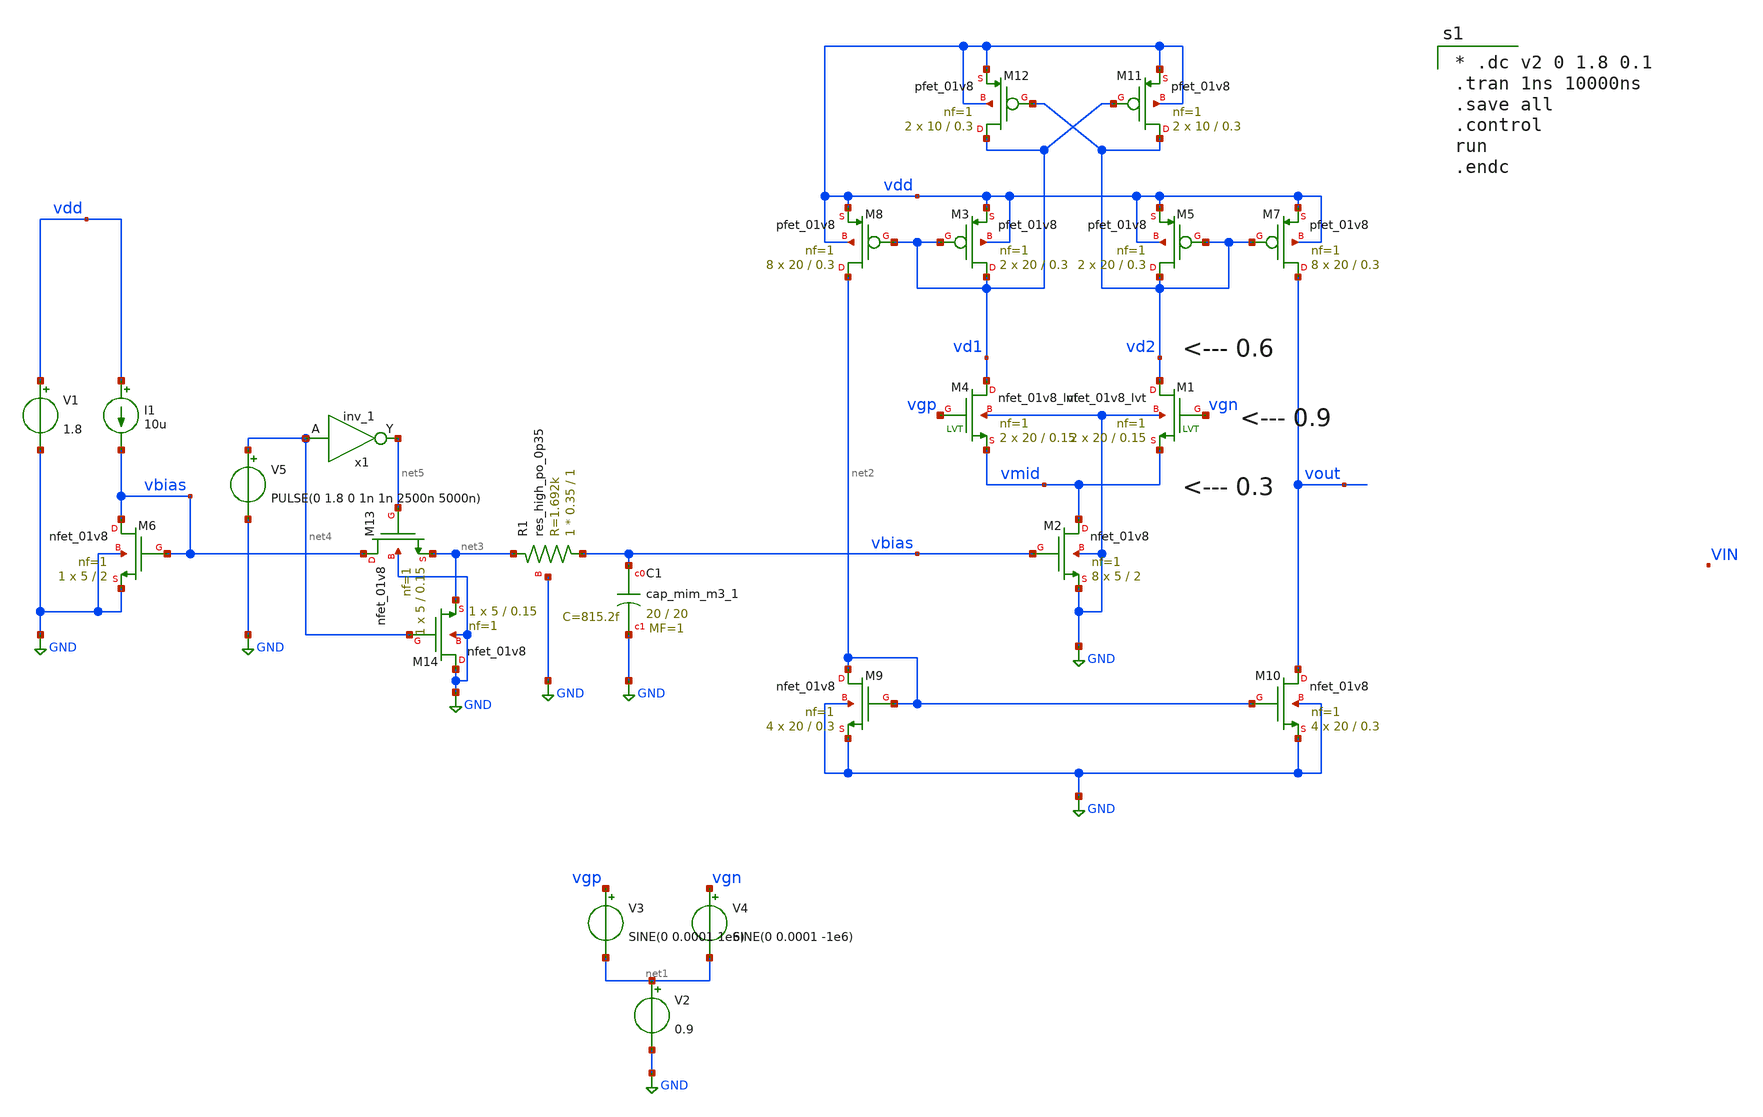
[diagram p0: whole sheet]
** sch_path: xschem/i_type_ota_tran_tb.sch
**.subckt i_type_ota_tran_tb
XM2 vmid vbias GND GND sky130_fd_pr__nfet_01v8 L=2 W=5 nf=1 ad='int((nf+1)/2) * W/nf * 0.29' as='int((nf+2)/2) * W/nf * 0.29'
+ pd='2*int((nf+1)/2) * (W/nf + 0.29)' ps='2*int((nf+2)/2) * (W/nf + 0.29)' nrd='0.29 / W' nrs='0.29 / W'
+ sa=0 sb=0 sd=0 mult=8 m=8
XM6 vbias vbias GND GND sky130_fd_pr__nfet_01v8 L=2 W=5 nf=1 ad='int((nf+1)/2) * W/nf * 0.29' as='int((nf+2)/2) * W/nf * 0.29'
+ pd='2*int((nf+1)/2) * (W/nf + 0.29)' ps='2*int((nf+2)/2) * (W/nf + 0.29)' nrd='0.29 / W' nrs='0.29 / W'
+ sa=0 sb=0 sd=0 mult=1 m=1
I1 vdd vbias 10u
XR1 vbias net3 GND sky130_fd_pr__res_high_po_0p35 L=1 mult=1 m=1
V1 vdd GND 1.8
V2 net1 GND 0.9
V3 vgp net1 SINE(0 0.0001 1e6)
XM4 vd1 vgp vmid GND sky130_fd_pr__nfet_01v8_lvt L=0.15 W=20 nf=1 ad='int((nf+1)/2) * W/nf * 0.29' as='int((nf+2)/2) * W/nf * 0.29'
+ pd='2*int((nf+1)/2) * (W/nf + 0.29)' ps='2*int((nf+2)/2) * (W/nf + 0.29)' nrd='0.29 / W' nrs='0.29 / W'
+ sa=0 sb=0 sd=0 mult=2 m=2
XM1 vd2 vgn vmid GND sky130_fd_pr__nfet_01v8_lvt L=0.15 W=20 nf=1 ad='int((nf+1)/2) * W/nf * 0.29' as='int((nf+2)/2) * W/nf * 0.29'
+ pd='2*int((nf+1)/2) * (W/nf + 0.29)' ps='2*int((nf+2)/2) * (W/nf + 0.29)' nrd='0.29 / W' nrs='0.29 / W'
+ sa=0 sb=0 sd=0 mult=2 m=2
XM3 vd1 vd1 vdd vdd sky130_fd_pr__pfet_01v8 L=0.3 W=20 nf=1 ad='int((nf+1)/2) * W/nf * 0.29' as='int((nf+2)/2) * W/nf * 0.29'
+ pd='2*int((nf+1)/2) * (W/nf + 0.29)' ps='2*int((nf+2)/2) * (W/nf + 0.29)' nrd='0.29 / W' nrs='0.29 / W'
+ sa=0 sb=0 sd=0 mult=2 m=2
XM5 vd2 vd2 vdd vdd sky130_fd_pr__pfet_01v8 L=0.3 W=20 nf=1 ad='int((nf+1)/2) * W/nf * 0.29' as='int((nf+2)/2) * W/nf * 0.29'
+ pd='2*int((nf+1)/2) * (W/nf + 0.29)' ps='2*int((nf+2)/2) * (W/nf + 0.29)' nrd='0.29 / W' nrs='0.29 / W'
+ sa=0 sb=0 sd=0 mult=2 m=2
XM7 vout vd2 vdd vdd sky130_fd_pr__pfet_01v8 L=0.3 W=20 nf=1 ad='int((nf+1)/2) * W/nf * 0.29' as='int((nf+2)/2) * W/nf * 0.29'
+ pd='2*int((nf+1)/2) * (W/nf + 0.29)' ps='2*int((nf+2)/2) * (W/nf + 0.29)' nrd='0.29 / W' nrs='0.29 / W'
+ sa=0 sb=0 sd=0 mult=8 m=8
XM8 net2 vd1 vdd vdd sky130_fd_pr__pfet_01v8 L=0.3 W=20 nf=1 ad='int((nf+1)/2) * W/nf * 0.29' as='int((nf+2)/2) * W/nf * 0.29'
+ pd='2*int((nf+1)/2) * (W/nf + 0.29)' ps='2*int((nf+2)/2) * (W/nf + 0.29)' nrd='0.29 / W' nrs='0.29 / W'
+ sa=0 sb=0 sd=0 mult=8 m=8
XM9 net2 net2 GND GND sky130_fd_pr__nfet_01v8 L=0.3 W=20 nf=1 ad='int((nf+1)/2) * W/nf * 0.29' as='int((nf+2)/2) * W/nf * 0.29'
+ pd='2*int((nf+1)/2) * (W/nf + 0.29)' ps='2*int((nf+2)/2) * (W/nf + 0.29)' nrd='0.29 / W' nrs='0.29 / W'
+ sa=0 sb=0 sd=0 mult=4 m=4
XM10 vout net2 GND GND sky130_fd_pr__nfet_01v8 L=0.3 W=20 nf=1 ad='int((nf+1)/2) * W/nf * 0.29' as='int((nf+2)/2) * W/nf * 0.29'
+ pd='2*int((nf+1)/2) * (W/nf + 0.29)' ps='2*int((nf+2)/2) * (W/nf + 0.29)' nrd='0.29 / W' nrs='0.29 / W'
+ sa=0 sb=0 sd=0 mult=4 m=4
XM11 vd2 vd1 vdd vdd sky130_fd_pr__pfet_01v8 L=0.3 W=10 nf=1 ad='int((nf+1)/2) * W/nf * 0.29' as='int((nf+2)/2) * W/nf * 0.29'
+ pd='2*int((nf+1)/2) * (W/nf + 0.29)' ps='2*int((nf+2)/2) * (W/nf + 0.29)' nrd='0.29 / W' nrs='0.29 / W'
+ sa=0 sb=0 sd=0 mult=2 m=2
XM12 vd1 vd2 vdd vdd sky130_fd_pr__pfet_01v8 L=0.3 W=10 nf=1 ad='int((nf+1)/2) * W/nf * 0.29' as='int((nf+2)/2) * W/nf * 0.29'
+ pd='2*int((nf+1)/2) * (W/nf + 0.29)' ps='2*int((nf+2)/2) * (W/nf + 0.29)' nrd='0.29 / W' nrs='0.29 / W'
+ sa=0 sb=0 sd=0 mult=2 m=2
V4 vgn net1 SINE(0 0.0001 -1e6)
XM13 vbias net5 net3 GND sky130_fd_pr__nfet_01v8 L=0.15 W=5 nf=1 ad='int((nf+1)/2) * W/nf * 0.29' as='int((nf+2)/2) * W/nf * 0.29'
+ pd='2*int((nf+1)/2) * (W/nf + 0.29)' ps='2*int((nf+2)/2) * (W/nf + 0.29)' nrd='0.29 / W' nrs='0.29 / W'
+ sa=0 sb=0 sd=0 mult=1 m=1
XM14 GND net4 net3 GND sky130_fd_pr__nfet_01v8 L=0.15 W=5 nf=1 ad='int((nf+1)/2) * W/nf * 0.29' as='int((nf+2)/2) * W/nf * 0.29'
+ pd='2*int((nf+1)/2) * (W/nf + 0.29)' ps='2*int((nf+2)/2) * (W/nf + 0.29)' nrd='0.29 / W' nrs='0.29 / W'
+ sa=0 sb=0 sd=0 mult=1 m=1
x1 net4 gnd gnd vdd vdd net5 sky130_fd_sc_hs__inv_1
V5 net4 GND PULSE(0 1.8 0 1n 1n 2500n 5000n)
XC1 vbias GND sky130_fd_pr__cap_mim_m3_1 W=20 L=20 MF=1 m=1
**** begin user architecture code
.lib $::SKYWATER_MODELS/sky130.lib.spice tt
.include $::PDKPATH/libs.ref/sky130_fd_sc_hs/spice/sky130_fd_sc_hs.spice


* .dc v2 0 1.8 0.1
.tran 1ns 10000ns
.save all
.control
run
.endc


**** end user architecture code
**.ends
.GLOBAL GND
.end
